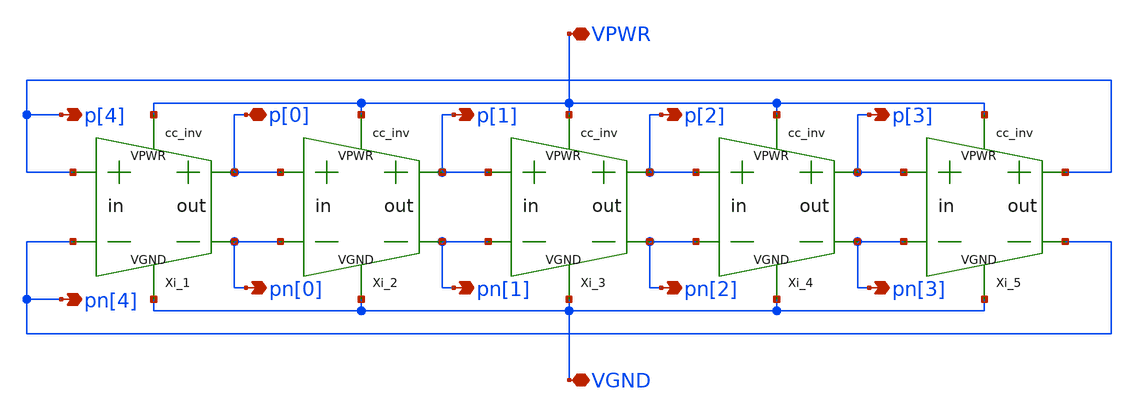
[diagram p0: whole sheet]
** sch_path: xschem/lib/5s_ringOsc.sch
**.subckt 5s_ringOsc VPWR VGND pn[0] p[0] pn[1] p[1] p[2] p[3] p[4] pn[2] pn[3] pn[4]
*.iopin VPWR
*.iopin VGND
*.opin pn[0]
*.iopin p[0]
*.opin pn[1]
*.opin p[1]
*.opin p[2]
*.opin p[3]
*.opin p[4]
*.opin pn[2]
*.opin pn[3]
*.opin pn[4]
Xi_1 p[4] pn[4] VPWR VGND p[0] pn[0] cc_inv L_main=1 L_aux=1 Wp=4 Wn=2
Xi_2 p[0] pn[0] VPWR VGND p[1] pn[1] cc_inv L_main=1 L_aux=1 Wp=4 Wn=2
Xi_3 p[1] pn[1] VPWR VGND p[2] pn[2] cc_inv L_main=1 L_aux=1 Wp=4 Wn=2
Xi_4 p[2] pn[2] VPWR VGND p[3] pn[3] cc_inv L_main=1 L_aux=1 Wp=4 Wn=2
Xi_5 p[3] pn[3] VPWR VGND p[4] pn[4] cc_inv L_main=1 L_aux=1 Wp=4 Wn=2
**.ends

* expanding   symbol:  cc_inv.sym # of pins=6
** sym_path: xschem/lib/cc_inv.sym
** sch_path: xschem/lib/cc_inv.sch
.subckt cc_inv inp inn VPWR VGND outp outn  L_main=1 L_aux=1 Wp=4 Wn=2
*.opin outp
*.ipin inn
*.iopin VGND
*.opin outn
*.ipin inp
*.iopin VPWR
Xi_1 inp VPWR VGND outp main_inv l="L_main" wp="Wp" wn="Wn"
Xi_2 inn VPWR VGND outn main_inv l="L_main" wp="Wp" wn="Wn"
Xi_3 outp VPWR VGND outn aux_inv L="L_aux" Wp="Wp" Wn="Wn"
Xi_4 outn VPWR VGND outp aux_inv L="L_aux" Wp="Wp" Wn="Wn"
.ends


* expanding   symbol:  main_inv.sym # of pins=4
** sym_path: main_inv.sym
** sch_path: main_inv.sch
.subckt main_inv A VPWR VGND Y  l=0.15 wp=1.2 wn=0.6
*.iopin VPWR
*.iopin VGND
*.ipin A
*.opin Y
XM1 Y A VPWR VDD sky130_fd_pr__pfet_01v8 L="L" W="Wp" nf=1 ad='int((1 + 1)/2) * "Wp" / 1 * 0.29' as='int((1 + 2)/2) * "Wp" / 1 * 0.29'
+ pd='2*int((1 + 1)/2) * ("Wp" / 1 + 0.29)' ps='2*int((1 + 2)/2) * ("Wp" / 1 + 0.29)' nrd='0.29 / "Wp" '
+ nrs='0.29 / "Wp" ' sa=0 sb=0 sd=0 mult=1 m=1
XM2 Y A VGND GND sky130_fd_pr__nfet_01v8 L="L" W="Wn" nf=1 ad='int((nf+1)/2) * W/nf * 0.29' as='int((nf+2)/2) * W/nf * 0.29'
+ pd='2*int((nf+1)/2) * (W/nf + 0.29)' ps='2*int((nf+2)/2) * (W/nf + 0.29)' nrd='0.29 / W' nrs='0.29 / W'
+ sa=0 sb=0 sd=0 mult=1 m=1
XM3 Y A VPWR VDD sky130_fd_pr__pfet_01v8 L="L" W="Wp" nf=1 ad='int((1 + 1)/2) * "Wp" / 1 * 0.29' as='int((1 + 2)/2) * "Wp" / 1 * 0.29'
+ pd='2*int((1 + 1)/2) * ("Wp" / 1 + 0.29)' ps='2*int((1 + 2)/2) * ("Wp" / 1 + 0.29)' nrd='0.29 / "Wp" '
+ nrs='0.29 / "Wp" ' sa=0 sb=0 sd=0 mult=1 m=1
XM4 Y A VGND GND sky130_fd_pr__nfet_01v8 L="L" W="Wn" nf=1 ad='int((nf+1)/2) * W/nf * 0.29' as='int((nf+2)/2) * W/nf * 0.29'
+ pd='2*int((nf+1)/2) * (W/nf + 0.29)' ps='2*int((nf+2)/2) * (W/nf + 0.29)' nrd='0.29 / W' nrs='0.29 / W'
+ sa=0 sb=0 sd=0 mult=1 m=1
XM5 Y A VPWR VDD sky130_fd_pr__pfet_01v8 L="L" W="Wp" nf=1 ad='int((1 + 1)/2) * "Wp" / 1 * 0.29' as='int((1 + 2)/2) * "Wp" / 1 * 0.29'
+ pd='2*int((1 + 1)/2) * ("Wp" / 1 + 0.29)' ps='2*int((1 + 2)/2) * ("Wp" / 1 + 0.29)' nrd='0.29 / "Wp" '
+ nrs='0.29 / "Wp" ' sa=0 sb=0 sd=0 mult=1 m=1
XM6 Y A VGND GND sky130_fd_pr__nfet_01v8 L="L" W="Wn" nf=1 ad='int((nf+1)/2) * W/nf * 0.29' as='int((nf+2)/2) * W/nf * 0.29'
+ pd='2*int((nf+1)/2) * (W/nf + 0.29)' ps='2*int((nf+2)/2) * (W/nf + 0.29)' nrd='0.29 / W' nrs='0.29 / W'
+ sa=0 sb=0 sd=0 mult=1 m=1
XM7 Y A VPWR VDD sky130_fd_pr__pfet_01v8 L="L" W="Wp" nf=1 ad='int((1 + 1)/2) * "Wp" / 1 * 0.29' as='int((1 + 2)/2) * "Wp" / 1 * 0.29'
+ pd='2*int((1 + 1)/2) * ("Wp" / 1 + 0.29)' ps='2*int((1 + 2)/2) * ("Wp" / 1 + 0.29)' nrd='0.29 / "Wp" '
+ nrs='0.29 / "Wp" ' sa=0 sb=0 sd=0 mult=1 m=1
XM8 Y A VGND GND sky130_fd_pr__nfet_01v8 L="L" W="Wn" nf=1 ad='int((nf+1)/2) * W/nf * 0.29' as='int((nf+2)/2) * W/nf * 0.29'
+ pd='2*int((nf+1)/2) * (W/nf + 0.29)' ps='2*int((nf+2)/2) * (W/nf + 0.29)' nrd='0.29 / W' nrs='0.29 / W'
+ sa=0 sb=0 sd=0 mult=1 m=1
.ends


* expanding   symbol:  aux_inv.sym # of pins=4
** sym_path: xschem/lib/aux_inv.sym
** sch_path: xschem/lib/aux_inv.sch
.subckt aux_inv A VPWR VGND Y  L=0.15 Wp=1.2 Wn=0.65
*.iopin VPWR
*.iopin VGND
*.ipin A
*.opin Y
XM1 Y A VPWR VDD sky130_fd_pr__pfet_01v8 L="L" W="Wp" nf=1 ad='int((1 + 1)/2) * "Wp" / 1 * 0.29' as='int((1 + 2)/2) * "Wp" / 1 * 0.29'
+ pd='2*int((1 + 1)/2) * ("Wp" / 1 + 0.29)' ps='2*int((1 + 2)/2) * ("Wp" / 1 + 0.29)' nrd='0.29 / "Wp" '
+ nrs='0.29 / "Wp" ' sa=0 sb=0 sd=0 mult=1 m=1
XM2 Y A VGND GND sky130_fd_pr__nfet_01v8 L="L" W="Wn" nf=1 ad='int((nf+1)/2) * W/nf * 0.29' as='int((nf+2)/2) * W/nf * 0.29'
+ pd='2*int((nf+1)/2) * (W/nf + 0.29)' ps='2*int((nf+2)/2) * (W/nf + 0.29)' nrd='0.29 / W' nrs='0.29 / W'
+ sa=0 sb=0 sd=0 mult=1 m=1
.ends

.end
